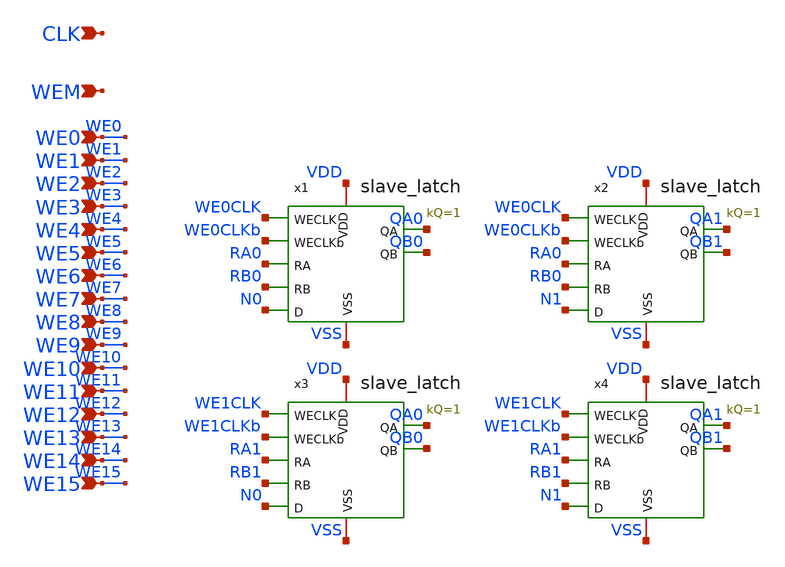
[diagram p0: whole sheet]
** sch_path: CAD3/rf.sch
**.subckt rf CLK WEM WE0 WE1 WE2 WE3 WE4 WE5 WE6 WE7 WE8 WE9 WE10 WE11 WE12 WE13 WE14 WE15
*.ipin CLK
*.ipin WEM
*.ipin WE0
*.ipin WE1
*.ipin WE2
*.ipin WE3
*.ipin WE4
*.ipin WE5
*.ipin WE6
*.ipin WE7
*.ipin WE8
*.ipin WE9
*.ipin WE10
*.ipin WE11
*.ipin WE12
*.ipin WE13
*.ipin WE14
*.ipin WE15
x1 VDD VSS QA0 WE0CLK WE0CLKb RA0 RB0 QB0 N0 slave_latch kQ=1
x2 VDD VSS QA1 WE0CLK WE0CLKb RA0 RB0 QB1 N1 slave_latch kQ=1
x3 VDD VSS QA0 WE1CLK WE1CLKb RA1 RB1 QB0 N0 slave_latch kQ=1
x4 VDD VSS QA1 WE1CLK WE1CLKb RA1 RB1 QB1 N1 slave_latch kQ=1
**.ends

* expanding   symbol:  engn1600-team1/CAD3/slave_latch.sym # of pins=9
** sym_path: CAD3/slave_latch.sym
** sch_path: CAD3/slave_latch.sch
.subckt slave_latch VDD VSS QA WECLK WECLKb RA RB QB D  kQ=1
*.ipin D
*.ipin RA
*.ipin RB
*.ipin WECLKb
*.ipin WECLK
*.opin QA
*.opin QB
*.iopin VDD
*.iopin VSS
XM1 net1 WECLKb net2 VDD pfet_03v3 L=0.28u W=0.22u nf=1 ad='int((nf+1)/2) * W/nf * 0.18u' as='int((nf+2)/2) * W/nf * 0.18u'
+ pd='2*int((nf+1)/2) * (W/nf + 0.18u)' ps='2*int((nf+2)/2) * (W/nf + 0.18u)' nrd='0.18u / W' nrs='0.18u / W'
+ sa=0 sb=0 sd=0 m=1
XM2 net1 D VDD VDD pfet_03v3 L=0.28u W=0.22u nf=1 ad='int((nf+1)/2) * W/nf * 0.18u' as='int((nf+2)/2) * W/nf * 0.18u'
+ pd='2*int((nf+1)/2) * (W/nf + 0.18u)' ps='2*int((nf+2)/2) * (W/nf + 0.18u)' nrd='0.18u / W' nrs='0.18u / W'
+ sa=0 sb=0 sd=0 m=1
XM3 net3 net2 VDD VDD pfet_03v3 L=0.28u W=0.22u nf=1 ad='int((nf+1)/2) * W/nf * 0.18u' as='int((nf+2)/2) * W/nf * 0.18u'
+ pd='2*int((nf+1)/2) * (W/nf + 0.18u)' ps='2*int((nf+2)/2) * (W/nf + 0.18u)' nrd='0.18u / W' nrs='0.18u / W'
+ sa=0 sb=0 sd=0 m=1
XM4 net4 net2 VDD VDD pfet_03v3 L=0.28u W=0.22u nf=1 ad='int((nf+1)/2) * W/nf * 0.18u' as='int((nf+2)/2) * W/nf * 0.18u'
+ pd='2*int((nf+1)/2) * (W/nf + 0.18u)' ps='2*int((nf+2)/2) * (W/nf + 0.18u)' nrd='0.18u / W' nrs='0.18u / W'
+ sa=0 sb=0 sd=0 m=1
XM5 VDD WECLK net8 VDD pfet_03v3 L=0.28u W=0.22u nf=1 ad='int((nf+1)/2) * W/nf * 0.18u' as='int((nf+2)/2) * W/nf * 0.18u'
+ pd='2*int((nf+1)/2) * (W/nf + 0.18u)' ps='2*int((nf+2)/2) * (W/nf + 0.18u)' nrd='0.18u / W' nrs='0.18u / W'
+ sa=0 sb=0 sd=0 m=1
XM6 net8 net4 net2 VDD pfet_03v3 L=0.28u W=0.22u nf=1 ad='int((nf+1)/2) * W/nf * 0.18u' as='int((nf+2)/2) * W/nf * 0.18u'
+ pd='2*int((nf+1)/2) * (W/nf + 0.18u)' ps='2*int((nf+2)/2) * (W/nf + 0.18u)' nrd='0.18u / W' nrs='0.18u / W'
+ sa=0 sb=0 sd=0 m=1
XM7 net1 D VSS VSS nfet_03v3 L=0.28u W=0.22u nf=1 ad='int((nf+1)/2) * W/nf * 0.18u' as='int((nf+2)/2) * W/nf * 0.18u'
+ pd='2*int((nf+1)/2) * (W/nf + 0.18u)' ps='2*int((nf+2)/2) * (W/nf + 0.18u)' nrd='0.18u / W' nrs='0.18u / W'
+ sa=0 sb=0 sd=0 m=1
XM8 net1 WECLK net2 VSS nfet_03v3 L=0.28u W=0.22u nf=1 ad='int((nf+1)/2) * W/nf * 0.18u' as='int((nf+2)/2) * W/nf * 0.18u'
+ pd='2*int((nf+1)/2) * (W/nf + 0.18u)' ps='2*int((nf+2)/2) * (W/nf + 0.18u)' nrd='0.18u / W' nrs='0.18u / W'
+ sa=0 sb=0 sd=0 m=1
XM9 net3 net2 VSS VSS nfet_03v3 L=0.28u W=0.22u nf=1 ad='int((nf+1)/2) * W/nf * 0.18u' as='int((nf+2)/2) * W/nf * 0.18u'
+ pd='2*int((nf+1)/2) * (W/nf + 0.18u)' ps='2*int((nf+2)/2) * (W/nf + 0.18u)' nrd='0.18u / W' nrs='0.18u / W'
+ sa=0 sb=0 sd=0 m=1
XM10 net4 net2 VSS VSS nfet_03v3 L=0.28u W=0.22u nf=1 ad='int((nf+1)/2) * W/nf * 0.18u' as='int((nf+2)/2) * W/nf * 0.18u'
+ pd='2*int((nf+1)/2) * (W/nf + 0.18u)' ps='2*int((nf+2)/2) * (W/nf + 0.18u)' nrd='0.18u / W' nrs='0.18u / W'
+ sa=0 sb=0 sd=0 m=1
XM11 net7 net4 net2 VSS nfet_03v3 L=0.28u W=0.22u nf=1 ad='int((nf+1)/2) * W/nf * 0.18u' as='int((nf+2)/2) * W/nf * 0.18u'
+ pd='2*int((nf+1)/2) * (W/nf + 0.18u)' ps='2*int((nf+2)/2) * (W/nf + 0.18u)' nrd='0.18u / W' nrs='0.18u / W'
+ sa=0 sb=0 sd=0 m=1
XM12 VSS WECLKb net7 VSS nfet_03v3 L=0.28u W=0.22u nf=1 ad='int((nf+1)/2) * W/nf * 0.18u' as='int((nf+2)/2) * W/nf * 0.18u'
+ pd='2*int((nf+1)/2) * (W/nf + 0.18u)' ps='2*int((nf+2)/2) * (W/nf + 0.18u)' nrd='0.18u / W' nrs='0.18u / W'
+ sa=0 sb=0 sd=0 m=1
XM13 net3 net5 QB VDD pfet_03v3 L=0.28u W=0.22u nf=1 ad='int((nf+1)/2) * W/nf * 0.18u' as='int((nf+2)/2) * W/nf * 0.18u'
+ pd='2*int((nf+1)/2) * (W/nf + 0.18u)' ps='2*int((nf+2)/2) * (W/nf + 0.18u)' nrd='0.18u / W' nrs='0.18u / W'
+ sa=0 sb=0 sd=0 m=1
XM14 net3 RB QB VSS nfet_03v3 L=0.28u W=0.22u nf=1 ad='int((nf+1)/2) * W/nf * 0.18u' as='int((nf+2)/2) * W/nf * 0.18u'
+ pd='2*int((nf+1)/2) * (W/nf + 0.18u)' ps='2*int((nf+2)/2) * (W/nf + 0.18u)' nrd='0.18u / W' nrs='0.18u / W'
+ sa=0 sb=0 sd=0 m=1
XM15 net5 RB VDD VDD pfet_03v3 L=0.28u W=0.22u nf=1 ad='int((nf+1)/2) * W/nf * 0.18u' as='int((nf+2)/2) * W/nf * 0.18u'
+ pd='2*int((nf+1)/2) * (W/nf + 0.18u)' ps='2*int((nf+2)/2) * (W/nf + 0.18u)' nrd='0.18u / W' nrs='0.18u / W'
+ sa=0 sb=0 sd=0 m=1
XM16 net5 RB VSS VSS nfet_03v3 L=0.28u W=0.22u nf=1 ad='int((nf+1)/2) * W/nf * 0.18u' as='int((nf+2)/2) * W/nf * 0.18u'
+ pd='2*int((nf+1)/2) * (W/nf + 0.18u)' ps='2*int((nf+2)/2) * (W/nf + 0.18u)' nrd='0.18u / W' nrs='0.18u / W'
+ sa=0 sb=0 sd=0 m=1
XM21 net3 net6 QA VDD pfet_03v3 L=0.28u W=0.22u nf=1 ad='int((nf+1)/2) * W/nf * 0.18u' as='int((nf+2)/2) * W/nf * 0.18u'
+ pd='2*int((nf+1)/2) * (W/nf + 0.18u)' ps='2*int((nf+2)/2) * (W/nf + 0.18u)' nrd='0.18u / W' nrs='0.18u / W'
+ sa=0 sb=0 sd=0 m=1
XM22 net3 RA QA VSS nfet_03v3 L=0.28u W=0.22u nf=1 ad='int((nf+1)/2) * W/nf * 0.18u' as='int((nf+2)/2) * W/nf * 0.18u'
+ pd='2*int((nf+1)/2) * (W/nf + 0.18u)' ps='2*int((nf+2)/2) * (W/nf + 0.18u)' nrd='0.18u / W' nrs='0.18u / W'
+ sa=0 sb=0 sd=0 m=1
XM23 net6 RA VDD VDD pfet_03v3 L=0.28u W=0.22u nf=1 ad='int((nf+1)/2) * W/nf * 0.18u' as='int((nf+2)/2) * W/nf * 0.18u'
+ pd='2*int((nf+1)/2) * (W/nf + 0.18u)' ps='2*int((nf+2)/2) * (W/nf + 0.18u)' nrd='0.18u / W' nrs='0.18u / W'
+ sa=0 sb=0 sd=0 m=1
XM24 net6 RA VSS VSS nfet_03v3 L=0.28u W=0.22u nf=1 ad='int((nf+1)/2) * W/nf * 0.18u' as='int((nf+2)/2) * W/nf * 0.18u'
+ pd='2*int((nf+1)/2) * (W/nf + 0.18u)' ps='2*int((nf+2)/2) * (W/nf + 0.18u)' nrd='0.18u / W' nrs='0.18u / W'
+ sa=0 sb=0 sd=0 m=1
.ends

.end
